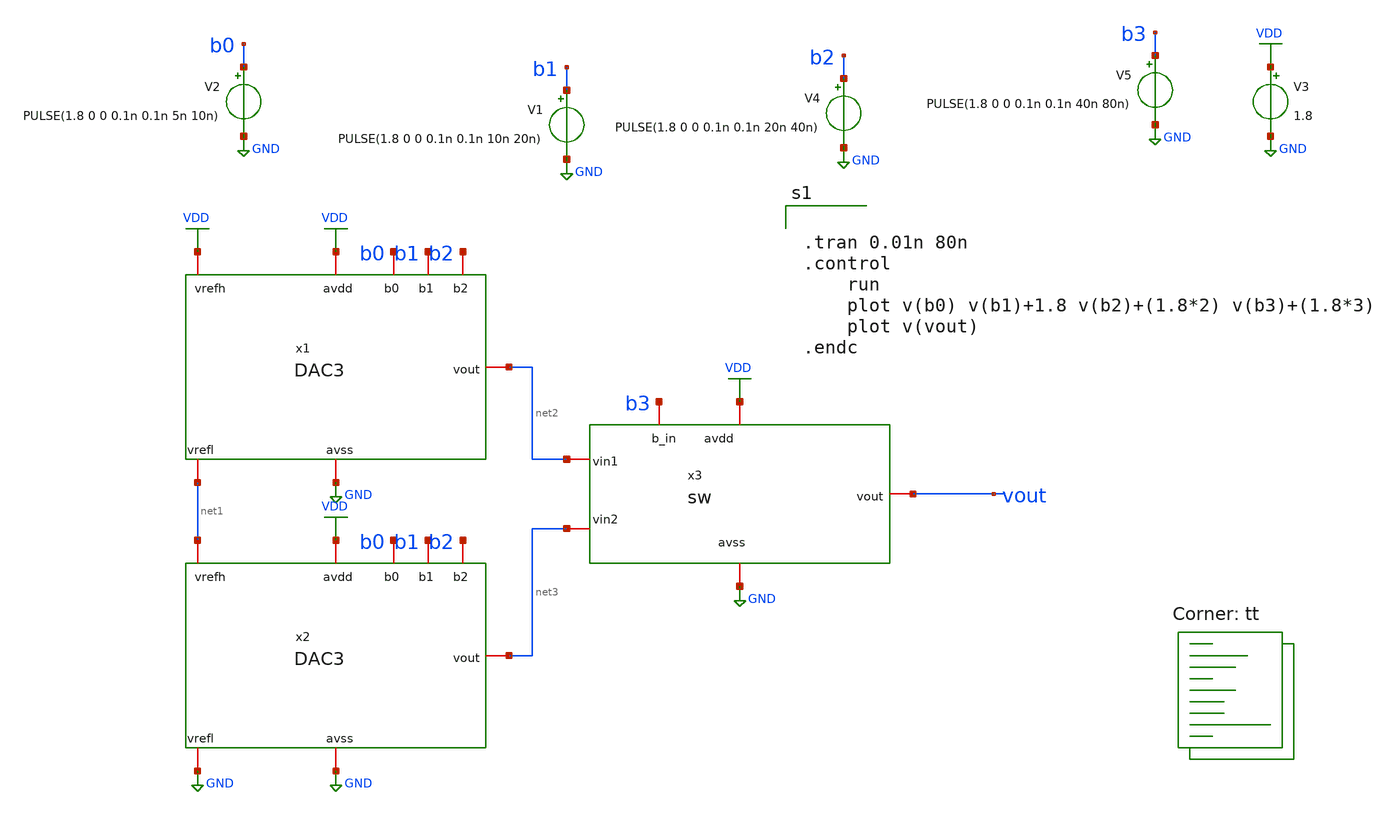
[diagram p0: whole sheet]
** sch_path: designs/libs/crossmem_ipn/dac4bits/sch/tb_DAC4BIT.sch
**.subckt tb_DAC4BIT
x1 VDD b0 b1 GND b2 VDD net2 net1 DAC3
x2 VDD b0 b1 GND b2 net1 net3 GND DAC3
x3 VDD b3 GND net2 vout net3 sw
V2 b0 GND PULSE(1.8 0 0 0.1n 0.1n 5n 10n)
V1 b1 GND PULSE(1.8 0 0 0.1n 0.1n 10n 20n)
V3 VDD GND 1.8
V4 b2 GND PULSE(1.8 0 0 0.1n 0.1n 20n 40n)
V5 b3 GND PULSE(1.8 0 0 0.1n 0.1n 40n 80n)
**** begin user architecture code


.tran 0.01n 80n
.control
	run
	plot v(b0) v(b1)+1.8 v(b2)+(1.8*2) v(b3)+(1.8*3)
	plot v(vout)
.endc



.lib $::SKYWATER_MODELS/sky130.lib.spice tt
**** end user architecture code
**.ends

* expanding   symbol:  DAC3.sym # of pins=8
** sym_path: designs/libs/crossmem_ipn/dac4bits/sch/DAC3.sym
** sch_path: designs/libs/crossmem_ipn/dac4bits/sch/DAC3.sch
.subckt DAC3 avdd b0 b1 avss b2 vrefh vout vrefl
*.iopin vrefh
*.iopin vrefl
*.iopin b0
*.iopin b1
*.iopin b2
*.iopin avdd
*.iopin avss
*.iopin vout
x1 b0 avdd b1 avss vrefh net1 net3 DAC2BIT
x2 b0 avdd b1 avss net3 net2 vrefl DAC2BIT
x3 avdd b2 avss net1 vout net2 sw
.ends


* expanding   symbol:  sw.sym # of pins=6
** sym_path: designs/libs/crossmem_ipn/dac4bits/sch/sw.sym
** sch_path: designs/libs/crossmem_ipn/dac4bits/sch/sw.sch
.subckt sw avdd b_in avss vin1 vout vin2
*.iopin avss
*.iopin vin1
*.iopin vout
*.iopin avdd
*.iopin vin2
*.iopin b_in
XM1 net1 b_in avss avss sky130_fd_pr__nfet_01v8 L=0.15 W=0.5 nf=1 ad='int((nf+1)/2) * W/nf * 0.29' as='int((nf+2)/2) * W/nf * 0.29'
+ pd='2*int((nf+1)/2) * (W/nf + 0.29)' ps='2*int((nf+2)/2) * (W/nf + 0.29)' nrd='0.29 / W' nrs='0.29 / W'
+ sa=0 sb=0 sd=0 mult=1 m=1
XM2 net1 b_in avdd avdd sky130_fd_pr__pfet_01v8 L=0.15 W=0.5 nf=1 ad='int((nf+1)/2) * W/nf * 0.29' as='int((nf+2)/2) * W/nf * 0.29'
+ pd='2*int((nf+1)/2) * (W/nf + 0.29)' ps='2*int((nf+2)/2) * (W/nf + 0.29)' nrd='0.29 / W' nrs='0.29 / W'
+ sa=0 sb=0 sd=0 mult=1 m=1
XM3 net2 net1 avss avss sky130_fd_pr__nfet_01v8 L=0.15 W=0.5 nf=1 ad='int((nf+1)/2) * W/nf * 0.29' as='int((nf+2)/2) * W/nf * 0.29'
+ pd='2*int((nf+1)/2) * (W/nf + 0.29)' ps='2*int((nf+2)/2) * (W/nf + 0.29)' nrd='0.29 / W' nrs='0.29 / W'
+ sa=0 sb=0 sd=0 mult=1 m=1
XM4 net2 net1 avdd avdd sky130_fd_pr__pfet_01v8 L=0.15 W=0.5 nf=1 ad='int((nf+1)/2) * W/nf * 0.29' as='int((nf+2)/2) * W/nf * 0.29'
+ pd='2*int((nf+1)/2) * (W/nf + 0.29)' ps='2*int((nf+2)/2) * (W/nf + 0.29)' nrd='0.29 / W' nrs='0.29 / W'
+ sa=0 sb=0 sd=0 mult=1 m=1
XM5 vout net1 vin1 avdd sky130_fd_pr__pfet_01v8 L=0.15 W=0.5 nf=1 ad='int((nf+1)/2) * W/nf * 0.29' as='int((nf+2)/2) * W/nf * 0.29'
+ pd='2*int((nf+1)/2) * (W/nf + 0.29)' ps='2*int((nf+2)/2) * (W/nf + 0.29)' nrd='0.29 / W' nrs='0.29 / W'
+ sa=0 sb=0 sd=0 mult=1 m=1
XM6 vout net1 vin2 avss sky130_fd_pr__nfet_01v8 L=0.15 W=0.5 nf=1 ad='int((nf+1)/2) * W/nf * 0.29' as='int((nf+2)/2) * W/nf * 0.29'
+ pd='2*int((nf+1)/2) * (W/nf + 0.29)' ps='2*int((nf+2)/2) * (W/nf + 0.29)' nrd='0.29 / W' nrs='0.29 / W'
+ sa=0 sb=0 sd=0 mult=1 m=1
XM7 vin1 net2 vout avss sky130_fd_pr__nfet_01v8 L=0.15 W=0.5 nf=1 ad='int((nf+1)/2) * W/nf * 0.29' as='int((nf+2)/2) * W/nf * 0.29'
+ pd='2*int((nf+1)/2) * (W/nf + 0.29)' ps='2*int((nf+2)/2) * (W/nf + 0.29)' nrd='0.29 / W' nrs='0.29 / W'
+ sa=0 sb=0 sd=0 mult=1 m=1
XM8 vin2 net2 vout avdd sky130_fd_pr__pfet_01v8 L=0.15 W=0.5 nf=1 ad='int((nf+1)/2) * W/nf * 0.29' as='int((nf+2)/2) * W/nf * 0.29'
+ pd='2*int((nf+1)/2) * (W/nf + 0.29)' ps='2*int((nf+2)/2) * (W/nf + 0.29)' nrd='0.29 / W' nrs='0.29 / W'
+ sa=0 sb=0 sd=0 mult=1 m=1
.ends


* expanding   symbol:  /foss/designs/crossmem_ipn/designs/libs/crossmem_ipn/dac4bits/sch/DAC2BIT.sym
*+ # of pins=7
** sym_path: designs/libs/crossmem_ipn/dac4bits/sch/DAC2BIT.sym
** sch_path: designs/libs/crossmem_ipn/dac4bits/sch/DAC2BIT.sch
.subckt DAC2BIT b0 avdd b1 avss vrefh vout vrefl
*.iopin vrefh
*.iopin vrefl
*.iopin b0
*.iopin b1
*.iopin avdd
*.iopin avss
*.iopin vout
x1 avdd b0 avss net5 net1 net4 sw
x2 avdd b0 avss net3 net2 vrefl sw
x3 avdd b1 avss net1 vout net2 sw
R5 net5 vrefh sky130_fd_pr__res_generic_l1 W=1 L=3.75 m=1
R6 net4 net5 sky130_fd_pr__res_generic_l1 W=1 L=3.75 m=1
R7 net3 net4 sky130_fd_pr__res_generic_l1 W=1 L=3.75 m=1
R8 vrefl net3 sky130_fd_pr__res_generic_l1 W=1 L=3.75 m=1
.ends

.GLOBAL GND
.GLOBAL VDD
.end
